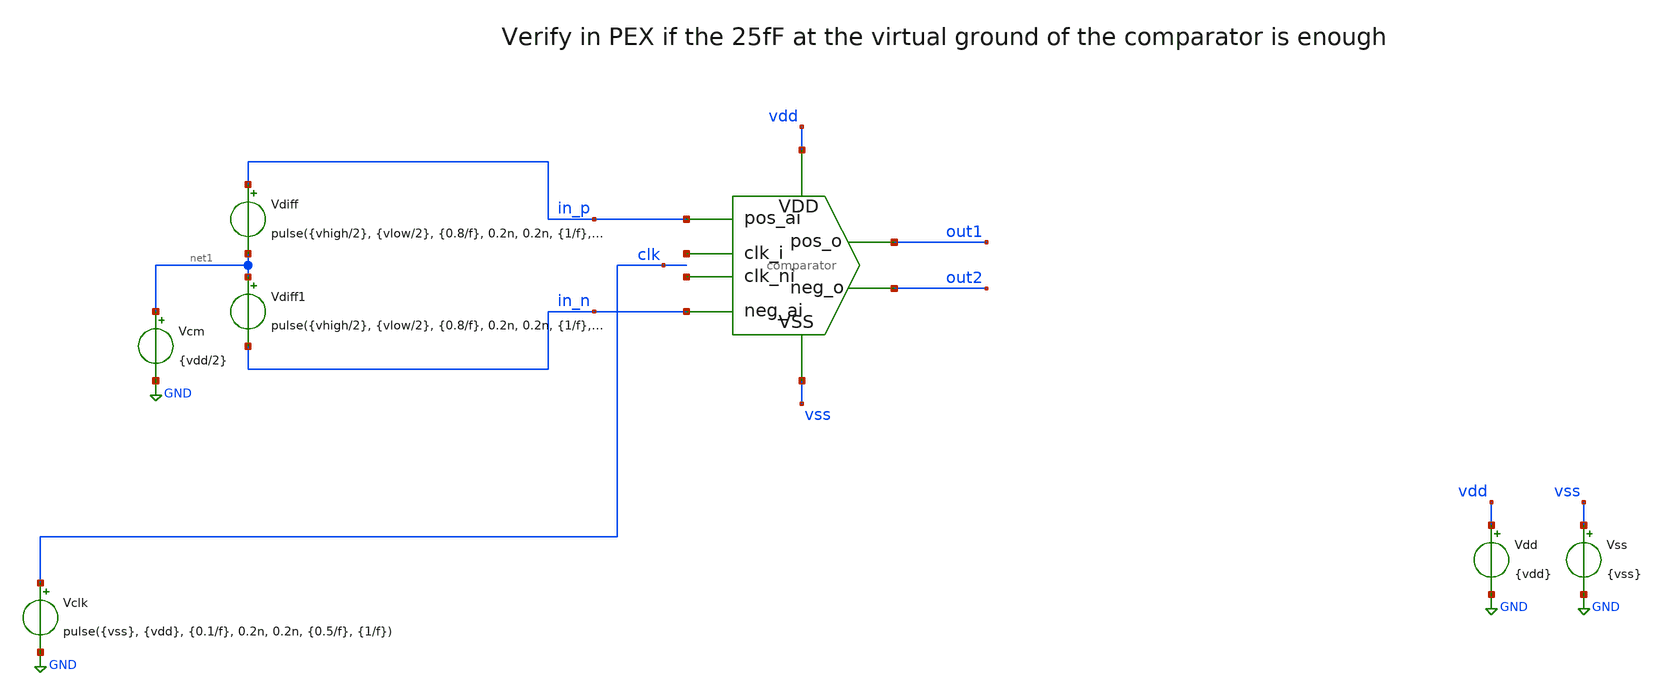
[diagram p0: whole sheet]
** sch_path: designs/comparator_debug/comparator_tb.sch
**.subckt comparator_tb
x1 net2 in_p in_n out2 out1 vss vdd net3 comparator
Vdd vdd GND {vdd}
Vss vss GND {vss}
Vclk clk GND pulse({vss}, {vdd}, {0.1/f}, 0.2n, 0.2n, {0.5/f}, {1/f})
Vdiff in_p net1 pulse({vhigh/2}, {vlow/2}, {0.8/f}, 0.2n, 0.2n, {1/f}, {2/f})
Vcm net1 GND {vdd/2}
Vdiff1 net1 in_n pulse({vhigh/2}, {vlow/2}, {0.8/f}, 0.2n, 0.2n, {1/f}, {2/f})
**** begin user architecture code

.lib $::SG13G2_MODELS/cornerMOSlv.lib mos_tt
.lib $::SG13G2_MODELS/cornerCAP.lib cap_typ
.include $::PDK_ROOT/ihp-sg13g2/libs.ref/sg13g2_stdcell/spice/sg13g2_stdcell.spice




.param vss=0
.param vdd=1.5
.param f=100Meg

.param vhigh=1.5m
.param vlow=-1.5m

.options maxstep=1p
.options method=gear2only
.options reltol=1e-4 vabstol=1e-6 iabstol=1e-12
.options cshunt=1f

.control
  save all
  tran 10p 49n
  write comparator_tb.raw
.endc



**** end user architecture code
**.ends

* expanding   symbol:  comparator.sym # of pins=8
** sym_path: designs/comparator_dt/comparator.sym
** sch_path: designs/comparator_dt/comparator.sch
.subckt comparator clk_i pos_ai neg_ai neg_o pos_o VSS VDD clk_ni
*.ipin pos_ai
*.ipin neg_ai
*.ipin VSS
*.ipin VDD
*.opin neg_o
*.opin pos_o
*.ipin clk_i
*.ipin clk_ni
XM12 neg_buf clk_i VDD VDD sg13_lv_pmos w=1.0u l=0.13u ng=1 m=1 mm_ok=1
XM13 pos_buf clk_i VDD VDD sg13_lv_pmos w=1.0u l=0.13u ng=1 m=1 mm_ok=1
XM14 net1 pos_ai neg_buf VSS sg13_lv_nmos w=1.0u l=0.13u ng=1 m=1 mm_ok=1
XM15 net1 neg_ai pos_buf VSS sg13_lv_nmos w=1.0u l=0.13u ng=1 m=1 mm_ok=1
XM16 VSS clk_i net1 VSS sg13_lv_nmos w=1.0u l=0.13u ng=1 m=1 mm_ok=1
XM17 net2 clk_ni VDD VDD sg13_lv_pmos w=2.0u l=0.13u ng=2 m=1 mm_ok=1
XM18 pos_o neg_o net2 VDD sg13_lv_pmos w=2.0u l=0.13u ng=2 m=1 mm_ok=1
XM19 neg_o pos_o net2 VDD sg13_lv_pmos w=2.0u l=0.13u ng=2 m=1 mm_ok=1
XM20 VSS neg_buf pos_o VSS sg13_lv_nmos w=1.0u l=0.13u ng=1 m=1 mm_ok=1
XM21 VSS neg_o pos_o VSS sg13_lv_nmos w=1.0u l=0.13u ng=1 m=1 mm_ok=1
XM22 VSS pos_o neg_o VSS sg13_lv_nmos w=1.0u l=0.13u ng=1 m=1 mm_ok=1
XM23 VSS pos_buf neg_o VSS sg13_lv_nmos w=1.0u l=0.13u ng=1 m=1 mm_ok=1
XC1 neg_buf VSS cap_cmim w=1.41e-5 l=1.41e-5 m=1 mm_ok=1
XC2 pos_buf VSS cap_cmim w=1.41e-5 l=1.41e-5 m=1 mm_ok=1
.ends

.GLOBAL GND
.end
